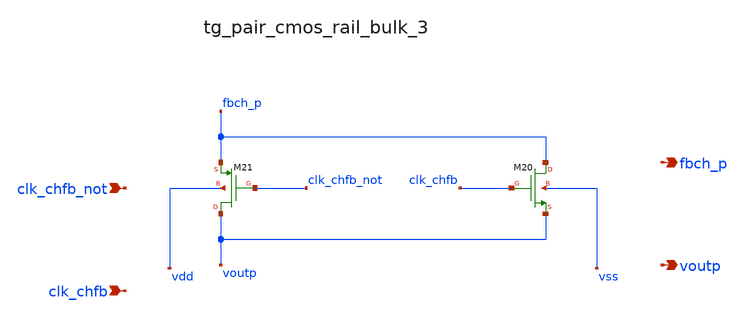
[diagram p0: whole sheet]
** sch_path: analog-db/raw/ia_003_fan_chopper_pf/hier/blocks/tg_pair_cmos_rail_bulk_3.sch
**.subckt tg_pair_cmos_rail_bulk_3 clk_chfb_not clk_chfb fbch_p voutp
*.ipin clk_chfb_not
*.ipin clk_chfb
*.opin fbch_p
*.opin voutp
XM20 fbch_p clk_chfb voutp vss sg13_lv_nmos w=x_dut_xm20_w l=x_dut_xm20_l ng=1 m=x_dut_xm20_m
XM21 voutp clk_chfb_not fbch_p vdd sg13_lv_pmos w=x_dut_xm21_w l=x_dut_xm21_l ng=1 m=x_dut_xm21_m
**.ends
.end
